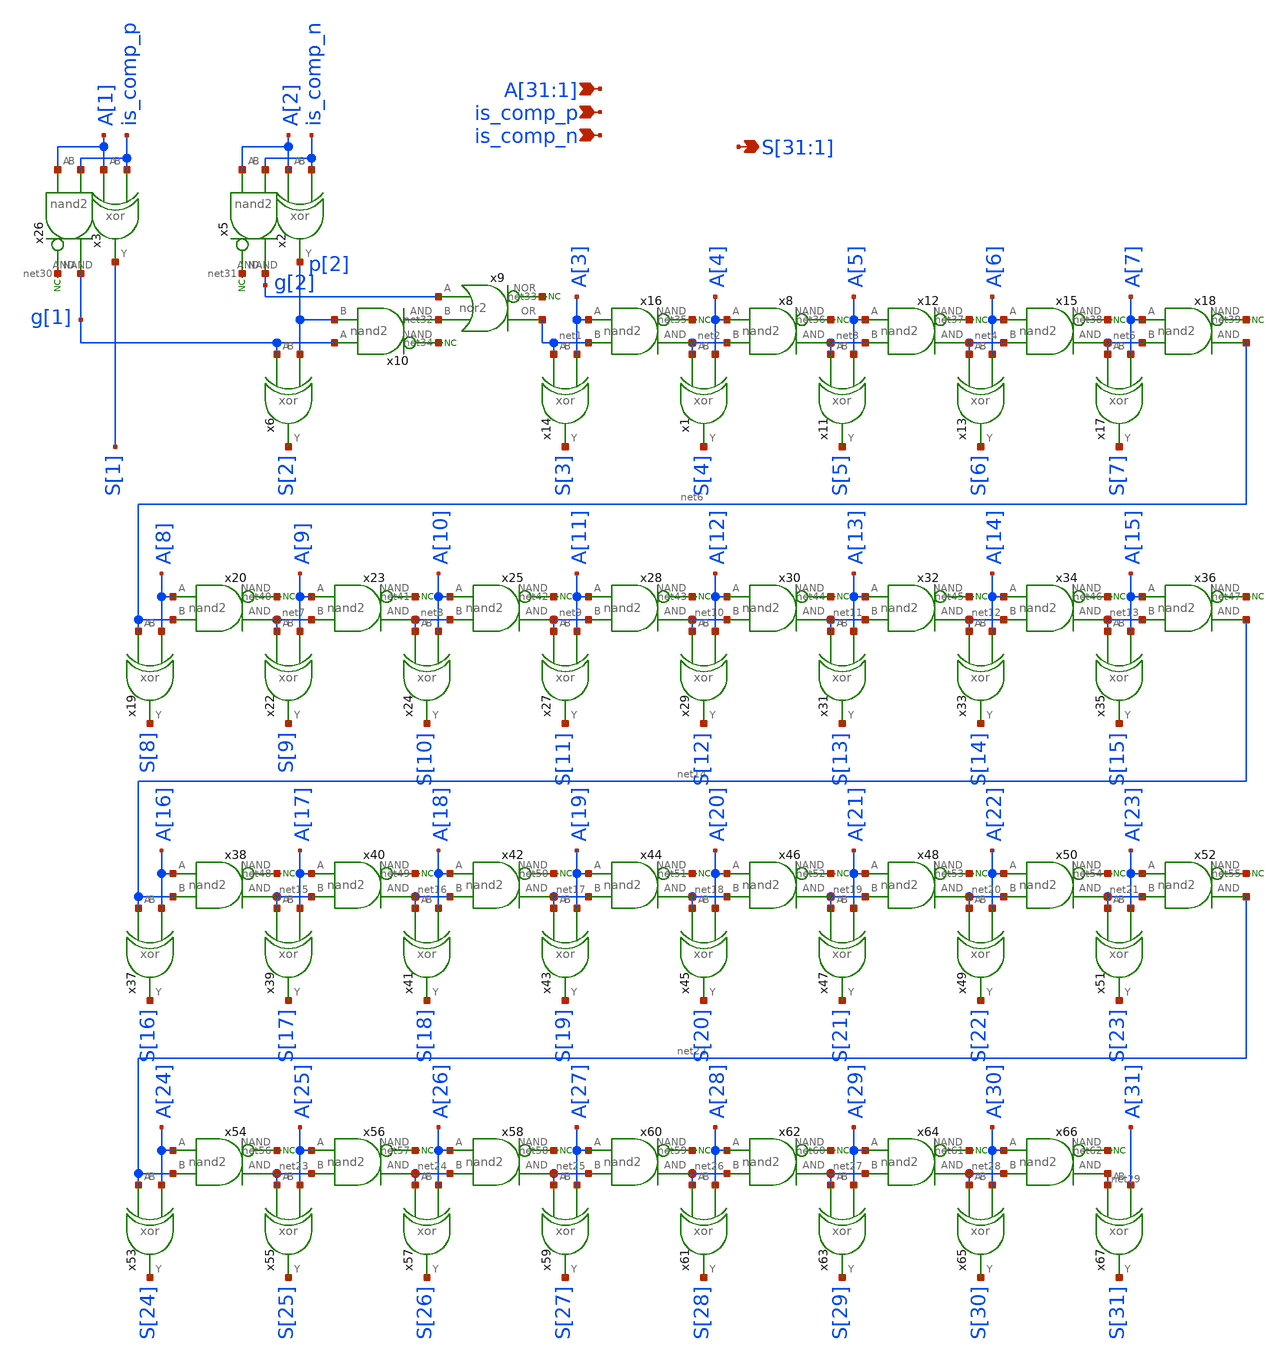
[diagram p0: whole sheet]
** sch_path: blocks/pc_inc/pc_inc.sch
**.subckt pc_inc
*+ S[31],S[30],S[29],S[28],S[27],S[26],S[25],S[24],S[23],S[22],S[21],S[20],S[19],S[18],S[17],S[16],S[15],S[14],S[13],S[12],S[11],S[10],S[9],S[8],S[7],S[6],S[5],S[4],S[3],S[2],S[1]
*+ A[31],A[30],A[29],A[28],A[27],A[26],A[25],A[24],A[23],A[22],A[21],A[20],A[19],A[18],A[17],A[16],A[15],A[14],A[13],A[12],A[11],A[10],A[9],A[8],A[7],A[6],A[5],A[4],A[3],A[2],A[1] is_comp_p is_comp_n
*.opin
*+ S[31],S[30],S[29],S[28],S[27],S[26],S[25],S[24],S[23],S[22],S[21],S[20],S[19],S[18],S[17],S[16],S[15],S[14],S[13],S[12],S[11],S[10],S[9],S[8],S[7],S[6],S[5],S[4],S[3],S[2],S[1]
*.ipin
*+ A[31],A[30],A[29],A[28],A[27],A[26],A[25],A[24],A[23],A[22],A[21],A[20],A[19],A[18],A[17],A[16],A[15],A[14],A[13],A[12],A[11],A[10],A[9],A[8],A[7],A[6],A[5],A[4],A[3],A[2],A[1]
*.ipin is_comp_p
*.ipin is_comp_n
x26 net30 g[1] A[1] is_comp_p nand2
* noconn #net30
x5 net31 g[2] A[2] is_comp_n nand2
* noconn #net31
x6 g[1] p[2] S[2] xor
x9 g[2] net1 net32 net33 nor2
x10 net34 net32 g[1] p[2] nand2
x14 net1 A[3] S[3] xor
x16 net35 net2 A[3] net1 nand2
* noconn #net34
* noconn #net33
* noconn #net35
x1 net2 A[4] S[4] xor
x8 net36 net3 A[4] net2 nand2
* noconn #net36
x11 net3 A[5] S[5] xor
x12 net37 net4 A[5] net3 nand2
* noconn #net37
x13 net4 A[6] S[6] xor
x15 net38 net5 A[6] net4 nand2
* noconn #net38
x17 net5 A[7] S[7] xor
x18 net39 net6 A[7] net5 nand2
* noconn #net39
x19 net6 A[8] S[8] xor
x20 net40 net7 A[8] net6 nand2
* noconn #net40
x22 net7 A[9] S[9] xor
x23 net41 net8 A[9] net7 nand2
* noconn #net41
x24 net8 A[10] S[10] xor
x25 net42 net9 A[10] net8 nand2
* noconn #net42
x27 net9 A[11] S[11] xor
x28 net43 net10 A[11] net9 nand2
* noconn #net43
x29 net10 A[12] S[12] xor
x30 net44 net11 A[12] net10 nand2
* noconn #net44
x31 net11 A[13] S[13] xor
x32 net45 net12 A[13] net11 nand2
* noconn #net45
x33 net12 A[14] S[14] xor
x34 net46 net13 A[14] net12 nand2
* noconn #net46
x35 net13 A[15] S[15] xor
x36 net47 net14 A[15] net13 nand2
* noconn #net47
x37 net14 A[16] S[16] xor
x38 net48 net15 A[16] net14 nand2
* noconn #net48
x39 net15 A[17] S[17] xor
x40 net49 net16 A[17] net15 nand2
* noconn #net49
x41 net16 A[18] S[18] xor
x42 net50 net17 A[18] net16 nand2
* noconn #net50
x43 net17 A[19] S[19] xor
x44 net51 net18 A[19] net17 nand2
* noconn #net51
x45 net18 A[20] S[20] xor
x46 net52 net19 A[20] net18 nand2
* noconn #net52
x47 net19 A[21] S[21] xor
x48 net53 net20 A[21] net19 nand2
* noconn #net53
x49 net20 A[22] S[22] xor
x50 net54 net21 A[22] net20 nand2
* noconn #net54
x51 net21 A[23] S[23] xor
x52 net55 net22 A[23] net21 nand2
* noconn #net55
x53 net22 A[24] S[24] xor
x54 net56 net23 A[24] net22 nand2
* noconn #net56
x55 net23 A[25] S[25] xor
x56 net57 net24 A[25] net23 nand2
* noconn #net57
x57 net24 A[26] S[26] xor
x58 net58 net25 A[26] net24 nand2
* noconn #net58
x59 net25 A[27] S[27] xor
x60 net59 net26 A[27] net25 nand2
* noconn #net59
x61 net26 A[28] S[28] xor
x62 net60 net27 A[28] net26 nand2
* noconn #net60
x63 net27 A[29] S[29] xor
x64 net61 net28 A[29] net27 nand2
* noconn #net61
x65 net28 A[30] S[30] xor
x66 net62 net29 A[30] net28 nand2
* noconn #net62
x67 net29 A[31] S[31] xor
x3 A[1] is_comp_p S[1] xor
x2 A[2] is_comp_n p[2] xor
**.ends
.end
